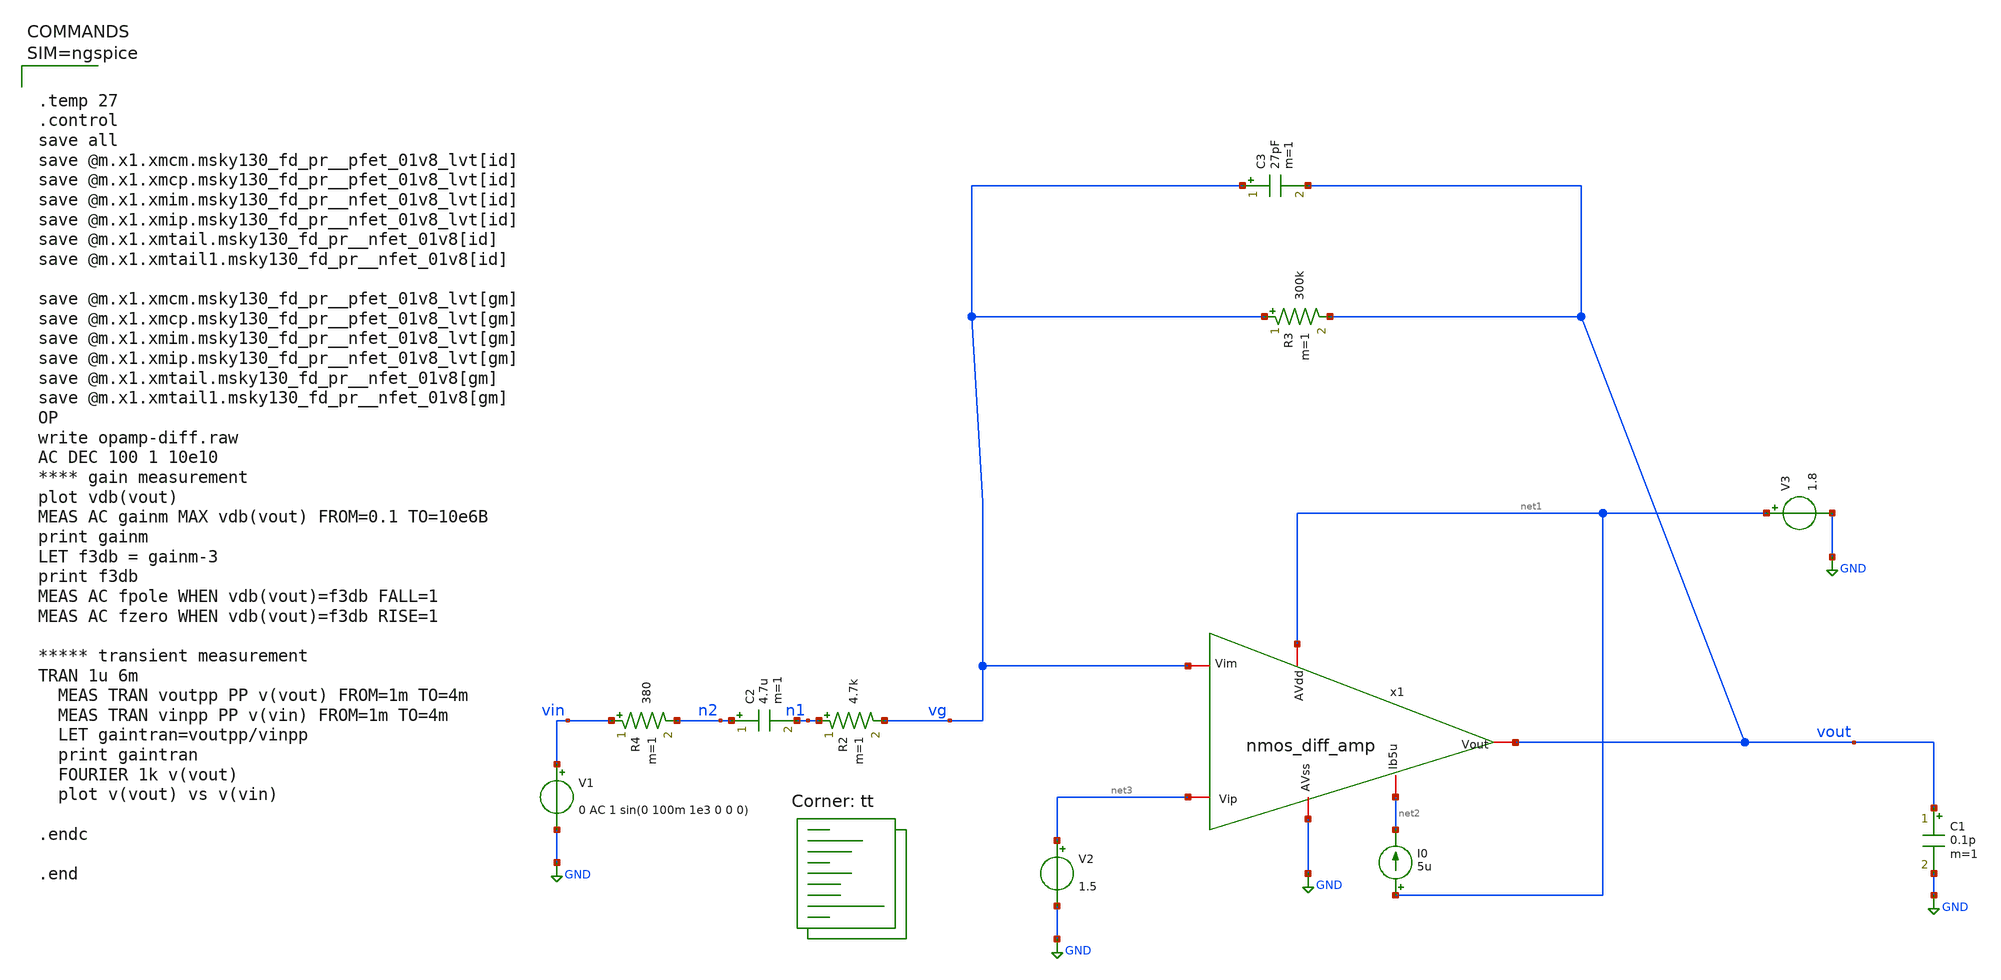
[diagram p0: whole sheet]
** sch_path: Work/xschem/opamp-diff.sch
**.subckt opamp-diff
V1 vin GND 0 AC 1 sin(0 100m 1e3 0 0 0)
V2 net3 GND 1.5
R2 n1 vg 4.7k m=1
R3 vg vout 300k m=1
C2 n2 n1 4.7u m=1
C3 vg vout 27pF m=1
R4 vin n2 380 m=1
V3 net1 GND 1.8
I0 net1 net2 5u
C1 vout GND 0.1p m=1
x1 net1 vout vg net3 net2 GND nmos_diff_amp
**** begin user architecture code



.temp 27
.control
save all
save @m.x1.xmcm.msky130_fd_pr__pfet_01v8_lvt[id]
save @m.x1.xmcp.msky130_fd_pr__pfet_01v8_lvt[id]
save @m.x1.xmim.msky130_fd_pr__nfet_01v8_lvt[id]
save @m.x1.xmip.msky130_fd_pr__nfet_01v8_lvt[id]
save @m.x1.xmtail.msky130_fd_pr__nfet_01v8[id]
save @m.x1.xmtail1.msky130_fd_pr__nfet_01v8[id]

save @m.x1.xmcm.msky130_fd_pr__pfet_01v8_lvt[gm]
save @m.x1.xmcp.msky130_fd_pr__pfet_01v8_lvt[gm]
save @m.x1.xmim.msky130_fd_pr__nfet_01v8_lvt[gm]
save @m.x1.xmip.msky130_fd_pr__nfet_01v8_lvt[gm]
save @m.x1.xmtail.msky130_fd_pr__nfet_01v8[gm]
save @m.x1.xmtail1.msky130_fd_pr__nfet_01v8[gm]
OP
write opamp-diff.raw
AC DEC 100 1 10e10
**** gain measurement
plot vdb(vout)
MEAS AC gainm MAX vdb(vout) FROM=0.1 TO=10e6B
print gainm
LET f3db = gainm-3
print f3db
MEAS AC fpole WHEN vdb(vout)=f3db FALL=1
MEAS AC fzero WHEN vdb(vout)=f3db RISE=1

***** transient measurement
TRAN 1u 6m
  MEAS TRAN voutpp PP v(vout) FROM=1m TO=4m
  MEAS TRAN vinpp PP v(vin) FROM=1m TO=4m
  LET gaintran=voutpp/vinpp
  print gaintran
  FOURIER 1k v(vout)
  plot v(vout) vs v(vin)

.endc

.end



.lib $::SKYWATER_MODELS/sky130.lib.spice tt
.lib /usr/local/share/pdk/sky130A/libs.tech/ngspice/sky130.lib.spice tt
**** end user architecture code
**.ends

* expanding   symbol:  nmos_diff_amp.sym # of pins=6
** sym_path: Work/xschem/nmos_diff_amp.sym
** sch_path: Work/xschem/nmos_diff_amp.sch
.subckt nmos_diff_amp AVdd Vout Vim Vip Ib5u AVss
*.iopin AVdd
*.iopin AVss
*.iopin Vim
*.iopin Vip
*.iopin Vout
*.iopin Ib5u
XMip vp Vip io io sky130_fd_pr__nfet_01v8_lvt L=2 W=5 nf=1 ad='int((1 + 1)/2) * 5 / 1 * 0.29' as='int((1 + 2)/2) * 5 / 1 * 0.29'
+ pd='2*int((1 + 1)/2) * (5 / 1 + 0.29)' ps='2*int((1 + 2)/2) * (5 / 1 + 0.29)' nrd='0.29 / 5 ' nrs='0.29 / 5 '
+ sa=0 sb=0 sd=0 mult=4 m=4
XMim Vout Vim io io sky130_fd_pr__nfet_01v8_lvt L=2 W=5 nf=1 ad='int((1 + 1)/2) * 5 / 1 * 0.29' as='int((1 + 2)/2) * 5 / 1 * 0.29'
+ pd='2*int((1 + 1)/2) * (5 / 1 + 0.29)' ps='2*int((1 + 2)/2) * (5 / 1 + 0.29)' nrd='0.29 / 5 ' nrs='0.29 / 5 '
+ sa=0 sb=0 sd=0 mult=4 m=4
XMcp vp vp AVdd AVdd sky130_fd_pr__pfet_01v8_lvt L=2 W=5 nf=1 ad='int((1 + 1)/2) * 5 / 1 * 0.29' as='int((1 + 2)/2) * 5 / 1 * 0.29'
+ pd='2*int((1 + 1)/2) * (5 / 1 + 0.29)' ps='2*int((1 + 2)/2) * (5 / 1 + 0.29)' nrd='0.29 / 5 ' nrs='0.29 / 5 '
+ sa=0 sb=0 sd=0 mult=2 m=2
XMcm Vout vp AVdd AVdd sky130_fd_pr__pfet_01v8_lvt L=2 W=5 nf=1 ad='int((1 + 1)/2) * 5 / 1 * 0.29' as='int((1 + 2)/2) * 5 / 1 * 0.29'
+ pd='2*int((1 + 1)/2) * (5 / 1 + 0.29)' ps='2*int((1 + 2)/2) * (5 / 1 + 0.29)' nrd='0.29 / 5 ' nrs='0.29 / 5 '
+ sa=0 sb=0 sd=0 mult=2 m=2
XMtail Ib5u Ib5u AVss AVss sky130_fd_pr__nfet_01v8 L=1 W=5 nf=1 ad='int((1 + 1)/2) * 5 / 1 * 0.29' as='int((1 + 2)/2) * 5 / 1 * 0.29'
+ pd='2*int((1 + 1)/2) * (5 / 1 + 0.29)' ps='2*int((1 + 2)/2) * (5 / 1 + 0.29)' nrd='0.29 / 5 ' nrs='0.29 / 5 '
+ sa=0 sb=0 sd=0 mult=1 m=1
XMtail1 io Ib5u AVss AVss sky130_fd_pr__nfet_01v8 L=1 W=5 nf=1 ad='int((1 + 1)/2) * 5 / 1 * 0.29' as='int((1 + 2)/2) * 5 / 1 * 0.29'
+ pd='2*int((1 + 1)/2) * (5 / 1 + 0.29)' ps='2*int((1 + 2)/2) * (5 / 1 + 0.29)' nrd='0.29 / 5 ' nrs='0.29 / 5 '
+ sa=0 sb=0 sd=0 mult=2 m=2
.ends

.GLOBAL GND
.end
